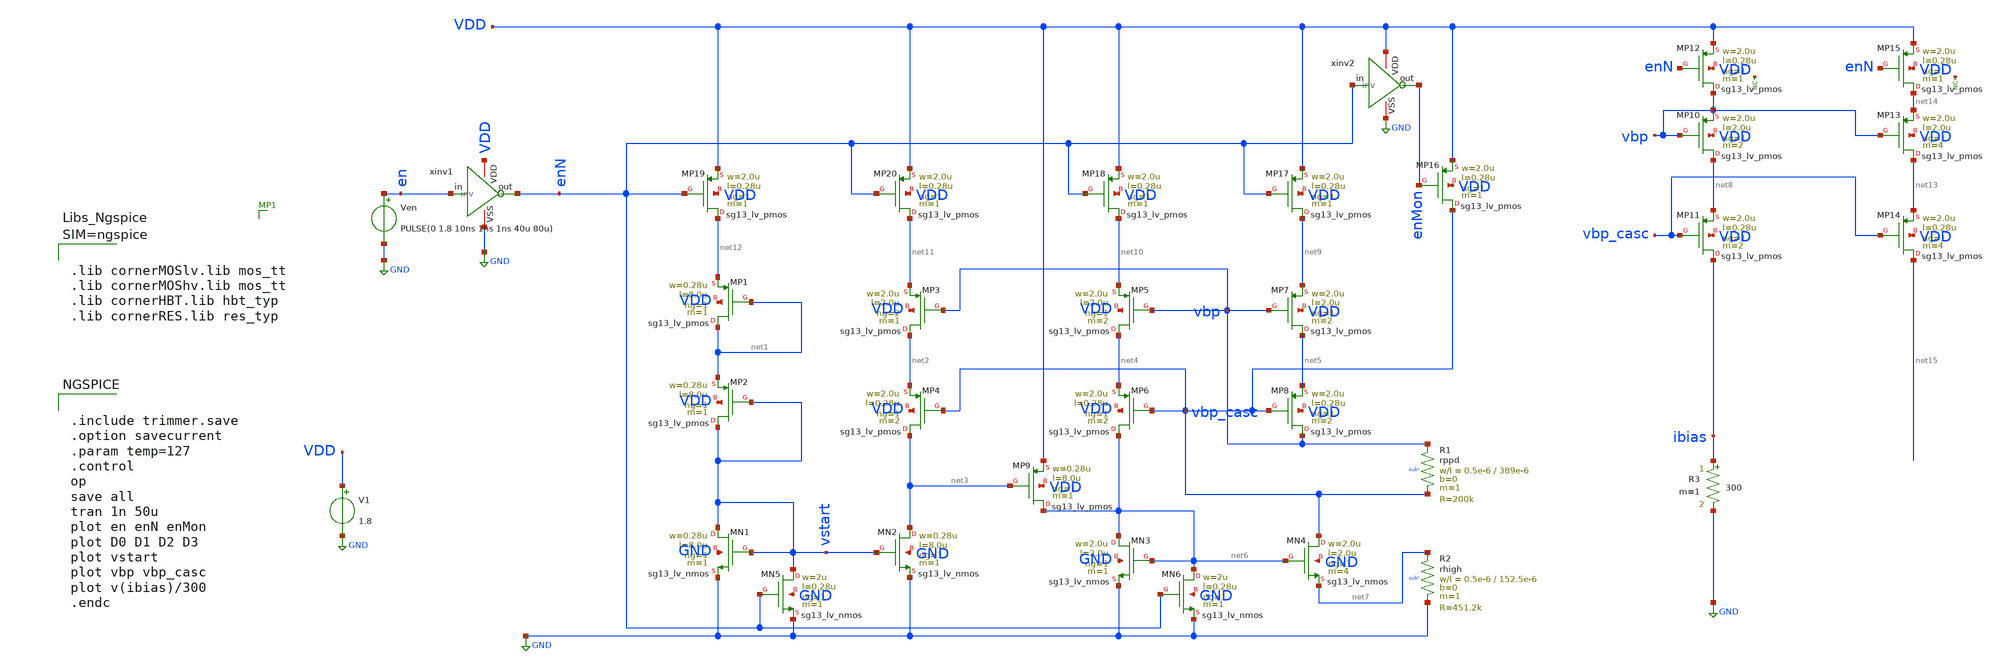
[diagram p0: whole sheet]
** sch_path: blocks/composite/dpi_adexp_neuron/design_data/xschem/trimmer.sch
**.subckt trimmer
XMP1 net1 net1 net12 VDD sg13_lv_pmos w=0.28u l=8.0u ng=1 m=1 mm_ok=1
XMP2 vstart vstart net1 VDD sg13_lv_pmos w=0.28u l=8.0u ng=1 m=1 mm_ok=1
XMN2 net3 vstart GND GND sg13_lv_nmos w=0.28u l=8.0u ng=1 m=1 mm_ok=1
XMN1 vstart vstart GND GND sg13_lv_nmos w=0.28u l=8.0u ng=1 m=1 mm_ok=1
XMP3 net2 vbp net11 VDD sg13_lv_pmos w=2.0u l=2.0u ng=2 m=1 mm_ok=1
XMP4 net3 vbp_casc net2 VDD sg13_lv_pmos w=2.0u l=0.28u ng=1 m=2 mm_ok=1
XMP5 net4 vbp net10 VDD sg13_lv_pmos w=2.0u l=2.0u ng=1 m=2 mm_ok=1
XMP6 net6 vbp_casc net4 VDD sg13_lv_pmos w=2.0u l=0.28u ng=1 m=2 mm_ok=1
XMP7 net5 vbp net9 VDD sg13_lv_pmos w=2.0u l=2.0u ng=1 m=2 mm_ok=1
XMP8 vbp vbp_casc net5 VDD sg13_lv_pmos w=2.0u l=0.28u ng=1 m=2 mm_ok=1
XMP9 net6 net3 VDD VDD sg13_lv_pmos w=0.28u l=8.0u ng=1 m=1 mm_ok=1
XMN3 net6 net6 GND GND sg13_lv_nmos w=2.0u l=2.0u ng=1 m=1 mm_ok=1
XMN4 vbp_casc net6 net7 GND sg13_lv_nmos w=2.0u l=2.0u ng=1 m=4 mm_ok=1
XR1 vbp vbp_casc sub! rppd w=0.5e-6 l=389e-6 m=1 b=0 mm_ok=1
XR2 net7 GND sub! rhigh w=0.5e-6 l=152.5e-6 m=1 b=0 mm_ok=1
R3 ibias GND 300 m=1
XMP10 net8 vbp vbp VDD sg13_lv_pmos w=2.0u l=2.0u ng=1 m=2 mm_ok=1
XMP11 ibias vbp_casc net8 VDD sg13_lv_pmos w=2.0u l=0.28u ng=1 m=2 mm_ok=1
XMP16 vbp_casc enMon VDD VDD sg13_lv_pmos w=2.0u l=0.28u ng=1 m=1 mm_ok=1
XMP17 net9 enN VDD VDD sg13_lv_pmos w=2.0u l=0.28u ng=1 m=1 mm_ok=1
XMP18 net10 enN VDD VDD sg13_lv_pmos w=2.0u l=0.28u ng=1 m=1 mm_ok=1
XMP19 net12 enN VDD VDD sg13_lv_pmos w=2.0u l=0.28u ng=1 m=1 mm_ok=1
XMP20 net11 enN VDD VDD sg13_lv_pmos w=2.0u l=0.28u ng=1 m=1 mm_ok=1
XMN5 vstart enN GND GND sg13_lv_nmos w=2u l=0.28u ng=1 m=1 mm_ok=1
XMN6 net6 enN GND GND sg13_lv_nmos w=2u l=0.28u ng=1 m=1 mm_ok=1
V1 VDD GND 1.8
Ven en GND PULSE(0 1.8 10ns 1ns 1ns 40u 80u)
xinv1 VDD en enN GND inv
xinv2 VDD enN enMon GND inv
XMP12 vbp enN VDD VDD sg13_lv_pmos w=2.0u l=0.28u ng=1 m=1 mm_ok=1
* noconn #net16
XMP13 net13 vbp net14 VDD sg13_lv_pmos w=2.0u l=2.0u ng=1 m=4 mm_ok=1
XMP14 net15 vbp_casc net13 VDD sg13_lv_pmos w=2.0u l=0.28u ng=1 m=4 mm_ok=1
XMP15 net14 enN VDD VDD sg13_lv_pmos w=2.0u l=0.28u ng=1 m=1 mm_ok=1
* noconn #net17
**** begin user architecture code


.include trimmer.save
.option savecurrent
.param temp=127
.control
op
save all
tran 1n 50u
plot en enN enMon
plot D0 D1 D2 D3
plot vstart
plot vbp vbp_casc
plot v(ibias)/300
.endc





.lib cornerMOSlv.lib mos_tt
.lib cornerMOShv.lib mos_tt
.lib cornerHBT.lib hbt_typ
.lib cornerRES.lib res_typ



**** end user architecture code
**.ends

* expanding   symbol:  inv.sym # of pins=4
** sym_path: blocks/composite/dpi_adexp_neuron/design_data/xschem/dev/inv.sym
** sch_path: blocks/composite/dpi_adexp_neuron/design_data/xschem/dev/inv.sch
.subckt inv VDD in out VSS
*.iopin VDD
*.ipin in
*.iopin VSS
*.opin out
XM1 out in VSS VSS sg13_lv_nmos w=2.0u l=0.28u ng=1 m=1 mm_ok=1
XM2 out in VDD VDD sg13_lv_pmos w=2.0u l=0.28u ng=1 m=1 mm_ok=1
.ends

.GLOBAL GND
.end
